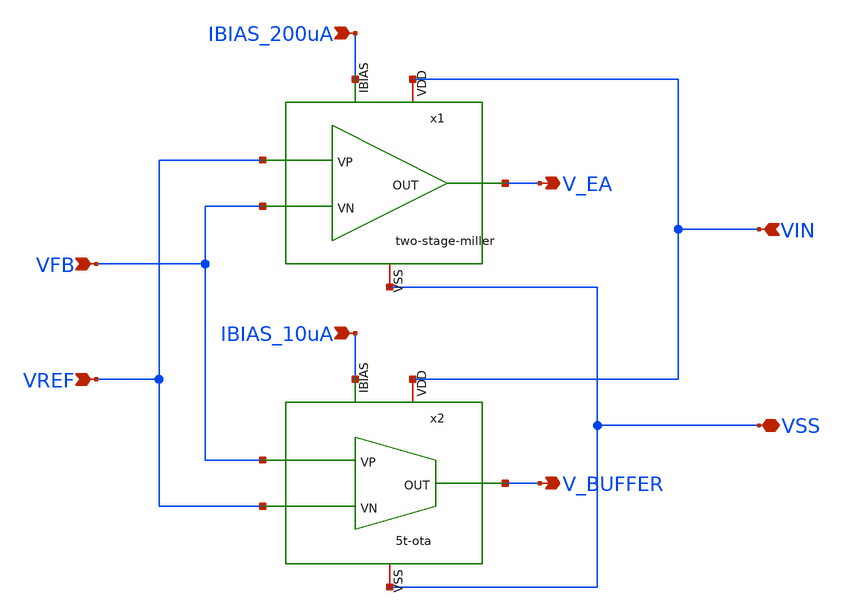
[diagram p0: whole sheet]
** sch_path: xschem/error-amplifier/schematics/error-amplifier-module.sch
**.subckt error-amplifier-module VFB VREF IBIAS_10uA IBIAS_200uA VIN V_EA VSS V_BUFFER
*.ipin VFB
*.ipin VREF
*.ipin IBIAS_10uA
*.ipin IBIAS_200uA
*.ipin VIN
*.opin V_EA
*.iopin VSS
*.opin V_BUFFER
x1 VIN V_EA VREF VFB IBIAS_200uA VSS two-stage-miller
x2 VIN V_BUFFER IBIAS_10uA VREF VFB VSS 5t-ota
**.ends

* expanding   symbol:  icdec-biomedical-pmic/xschem/error-amplifier/schematics/two-stage-miller.sym
*+ # of pins=6
** sym_path: xschem/error-amplifier/schematics/two-stage-miller.sym
** sch_path: xschem/error-amplifier/schematics/two-stage-miller.sch
.subckt two-stage-miller VDD OUT VP VN IBIAS VSS
*.iopin VDD
*.iopin VSS
*.ipin IBIAS
*.ipin VP
*.ipin VN
*.opin OUT
XM1 net3 net2 VDD VDD sky130_fd_pr__pfet_g5v0d10v5 L=1.25 W=75.2 nf=8 ad='int((nf+1)/2) * W/nf * 0.29'
+ as='int((nf+2)/2) * W/nf * 0.29' pd='2*int((nf+1)/2) * (W/nf + 0.29)' ps='2*int((nf+2)/2) * (W/nf + 0.29)'
+ nrd='0.29 / W' nrs='0.29 / W' sa=0 sb=0 sd=0 mult=1 m=1
XM2 net2 net2 VDD VDD sky130_fd_pr__pfet_g5v0d10v5 L=1.25 W=75.2 nf=8 ad='int((nf+1)/2) * W/nf * 0.29'
+ as='int((nf+2)/2) * W/nf * 0.29' pd='2*int((nf+1)/2) * (W/nf + 0.29)' ps='2*int((nf+2)/2) * (W/nf + 0.29)'
+ nrd='0.29 / W' nrs='0.29 / W' sa=0 sb=0 sd=0 mult=1 m=1
XM3 net3 VN net1 VSS sky130_fd_pr__nfet_g5v0d10v5 L=0.5 W=37.7 nf=8 ad='int((nf+1)/2) * W/nf * 0.29'
+ as='int((nf+2)/2) * W/nf * 0.29' pd='2*int((nf+1)/2) * (W/nf + 0.29)' ps='2*int((nf+2)/2) * (W/nf + 0.29)'
+ nrd='0.29 / W' nrs='0.29 / W' sa=0 sb=0 sd=0 mult=1 m=1
XM4 net2 VP net1 VSS sky130_fd_pr__nfet_g5v0d10v5 L=0.5 W=37.7 nf=8 ad='int((nf+1)/2) * W/nf * 0.29'
+ as='int((nf+2)/2) * W/nf * 0.29' pd='2*int((nf+1)/2) * (W/nf + 0.29)' ps='2*int((nf+2)/2) * (W/nf + 0.29)'
+ nrd='0.29 / W' nrs='0.29 / W' sa=0 sb=0 sd=0 mult=1 m=1
XM5 net1 IBIAS VSS VSS sky130_fd_pr__nfet_g5v0d10v5 L=1.25 W=60 nf=8 ad='int((nf+1)/2) * W/nf * 0.29'
+ as='int((nf+2)/2) * W/nf * 0.29' pd='2*int((nf+1)/2) * (W/nf + 0.29)' ps='2*int((nf+2)/2) * (W/nf + 0.29)'
+ nrd='0.29 / W' nrs='0.29 / W' sa=0 sb=0 sd=0 mult=1 m=1
XM6 IBIAS IBIAS VSS VSS sky130_fd_pr__nfet_g5v0d10v5 L=1.25 W=60 nf=8 ad='int((nf+1)/2) * W/nf * 0.29'
+ as='int((nf+2)/2) * W/nf * 0.29' pd='2*int((nf+1)/2) * (W/nf + 0.29)' ps='2*int((nf+2)/2) * (W/nf + 0.29)'
+ nrd='0.29 / W' nrs='0.29 / W' sa=0 sb=0 sd=0 mult=1 m=1
XM7 OUT net3 VDD VDD sky130_fd_pr__pfet_g5v0d10v5 L=1.25 W=160 nf=16 ad='int((nf+1)/2) * W/nf * 0.29'
+ as='int((nf+2)/2) * W/nf * 0.29' pd='2*int((nf+1)/2) * (W/nf + 0.29)' ps='2*int((nf+2)/2) * (W/nf + 0.29)'
+ nrd='0.29 / W' nrs='0.29 / W' sa=0 sb=0 sd=0 mult=1 m=1
XM8 OUT IBIAS VSS VSS sky130_fd_pr__nfet_g5v0d10v5 L=1.25 W=60 nf=8 ad='int((nf+1)/2) * W/nf * 0.29'
+ as='int((nf+2)/2) * W/nf * 0.29' pd='2*int((nf+1)/2) * (W/nf + 0.29)' ps='2*int((nf+2)/2) * (W/nf + 0.29)'
+ nrd='0.29 / W' nrs='0.29 / W' sa=0 sb=0 sd=0 mult=1 m=1
XC1 net4 net3 sky130_fd_pr__cap_mim_m3_1 W=25 L=25 MF=8 m=8
XM9 OUT VSS net4 VDD sky130_fd_pr__pfet_g5v0d10v5 L=0.9 W=20 nf=4 ad='int((nf+1)/2) * W/nf * 0.29' as='int((nf+2)/2) * W/nf * 0.29'
+ pd='2*int((nf+1)/2) * (W/nf + 0.29)' ps='2*int((nf+2)/2) * (W/nf + 0.29)' nrd='0.29 / W' nrs='0.29 / W'
+ sa=0 sb=0 sd=0 mult=1 m=1
.ends


* expanding   symbol:  icdec-biomedical-pmic/xschem/5t-ota/schematics/5t-ota.sym # of pins=6
** sym_path: xschem/5t-ota/schematics/5t-ota.sym
** sch_path: xschem/5t-ota/schematics/5t-ota.sch
.subckt 5t-ota VDD OUT IBIAS VN VP VSS
*.ipin VP
*.ipin VN
*.ipin IBIAS
*.iopin VDD
*.iopin VSS
*.opin OUT
XM1 net1 VP net2 VSS sky130_fd_pr__nfet_g5v0d10v5 L=0.75 W=8.5 nf=1 ad='int((nf+1)/2) * W/nf * 0.29'
+ as='int((nf+2)/2) * W/nf * 0.29' pd='2*int((nf+1)/2) * (W/nf + 0.29)' ps='2*int((nf+2)/2) * (W/nf + 0.29)'
+ nrd='0.29 / W' nrs='0.29 / W' sa=0 sb=0 sd=0 mult=1 m=1
XM2 OUT VN net2 VSS sky130_fd_pr__nfet_g5v0d10v5 L=0.75 W=8.5 nf=1 ad='int((nf+1)/2) * W/nf * 0.29' as='int((nf+2)/2) * W/nf * 0.29'
+ pd='2*int((nf+1)/2) * (W/nf + 0.29)' ps='2*int((nf+2)/2) * (W/nf + 0.29)' nrd='0.29 / W' nrs='0.29 / W'
+ sa=0 sb=0 sd=0 mult=1 m=1
XM3 net2 IBIAS VSS VSS sky130_fd_pr__nfet_g5v0d10v5 L=1.25 W=1.58 nf=1 ad='int((nf+1)/2) * W/nf * 0.29'
+ as='int((nf+2)/2) * W/nf * 0.29' pd='2*int((nf+1)/2) * (W/nf + 0.29)' ps='2*int((nf+2)/2) * (W/nf + 0.29)'
+ nrd='0.29 / W' nrs='0.29 / W' sa=0 sb=0 sd=0 mult=1 m=1
XM4 OUT net1 VDD VDD sky130_fd_pr__pfet_g5v0d10v5 L=1.25 W=4.85 nf=1 ad='int((nf+1)/2) * W/nf * 0.29'
+ as='int((nf+2)/2) * W/nf * 0.29' pd='2*int((nf+1)/2) * (W/nf + 0.29)' ps='2*int((nf+2)/2) * (W/nf + 0.29)'
+ nrd='0.29 / W' nrs='0.29 / W' sa=0 sb=0 sd=0 mult=1 m=1
XM5 net1 net1 VDD VDD sky130_fd_pr__pfet_g5v0d10v5 L=1.25 W=4.85 nf=1 ad='int((nf+1)/2) * W/nf * 0.29'
+ as='int((nf+2)/2) * W/nf * 0.29' pd='2*int((nf+1)/2) * (W/nf + 0.29)' ps='2*int((nf+2)/2) * (W/nf + 0.29)'
+ nrd='0.29 / W' nrs='0.29 / W' sa=0 sb=0 sd=0 mult=1 m=1
XM6 IBIAS IBIAS VSS VSS sky130_fd_pr__nfet_g5v0d10v5 L=1.25 W=1.58 nf=1 ad='int((nf+1)/2) * W/nf * 0.29'
+ as='int((nf+2)/2) * W/nf * 0.29' pd='2*int((nf+1)/2) * (W/nf + 0.29)' ps='2*int((nf+2)/2) * (W/nf + 0.29)'
+ nrd='0.29 / W' nrs='0.29 / W' sa=0 sb=0 sd=0 mult=1 m=1
.ends

.end
